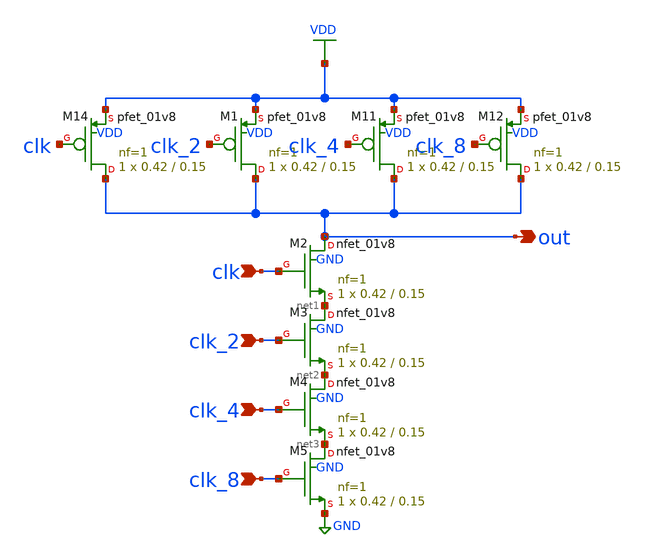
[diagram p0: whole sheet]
** sch_path: xschem/and_set/and_4.sch
**.subckt and_4 clk_2 clk clk_4 clk_8 out
*.ipin clk_2
*.ipin clk
*.ipin clk_4
*.ipin clk_8
*.opin out
XM1 out clk_2 VDD VDD sky130_fd_pr__pfet_01v8 L=0.15 W=0.42 nf=1 ad='int((nf+1)/2) * W/nf * 0.29' as='int((nf+2)/2) * W/nf * 0.29'
+ pd='2*int((nf+1)/2) * (W/nf + 0.29)' ps='2*int((nf+2)/2) * (W/nf + 0.29)' nrd='0.29 / W' nrs='0.29 / W'
+ sa=0 sb=0 sd=0 mult=1 m=1
XM2 out clk net1 GND sky130_fd_pr__nfet_01v8 L=0.15 W=0.42 nf=1 ad='int((nf+1)/2) * W/nf * 0.29' as='int((nf+2)/2) * W/nf * 0.29'
+ pd='2*int((nf+1)/2) * (W/nf + 0.29)' ps='2*int((nf+2)/2) * (W/nf + 0.29)' nrd='0.29 / W' nrs='0.29 / W'
+ sa=0 sb=0 sd=0 mult=1 m=1
XM3 net1 clk_2 net2 GND sky130_fd_pr__nfet_01v8 L=0.15 W=0.42 nf=1 ad='int((nf+1)/2) * W/nf * 0.29' as='int((nf+2)/2) * W/nf * 0.29'
+ pd='2*int((nf+1)/2) * (W/nf + 0.29)' ps='2*int((nf+2)/2) * (W/nf + 0.29)' nrd='0.29 / W' nrs='0.29 / W'
+ sa=0 sb=0 sd=0 mult=1 m=1
XM4 net2 clk_4 net3 GND sky130_fd_pr__nfet_01v8 L=0.15 W=0.42 nf=1 ad='int((nf+1)/2) * W/nf * 0.29' as='int((nf+2)/2) * W/nf * 0.29'
+ pd='2*int((nf+1)/2) * (W/nf + 0.29)' ps='2*int((nf+2)/2) * (W/nf + 0.29)' nrd='0.29 / W' nrs='0.29 / W'
+ sa=0 sb=0 sd=0 mult=1 m=1
XM5 net3 clk_8 GND GND sky130_fd_pr__nfet_01v8 L=0.15 W=0.42 nf=1 ad='int((nf+1)/2) * W/nf * 0.29' as='int((nf+2)/2) * W/nf * 0.29'
+ pd='2*int((nf+1)/2) * (W/nf + 0.29)' ps='2*int((nf+2)/2) * (W/nf + 0.29)' nrd='0.29 / W' nrs='0.29 / W'
+ sa=0 sb=0 sd=0 mult=1 m=1
XM11 out clk_4 VDD VDD sky130_fd_pr__pfet_01v8 L=0.15 W=0.42 nf=1 ad='int((nf+1)/2) * W/nf * 0.29' as='int((nf+2)/2) * W/nf * 0.29'
+ pd='2*int((nf+1)/2) * (W/nf + 0.29)' ps='2*int((nf+2)/2) * (W/nf + 0.29)' nrd='0.29 / W' nrs='0.29 / W'
+ sa=0 sb=0 sd=0 mult=1 m=1
XM12 out clk_8 VDD VDD sky130_fd_pr__pfet_01v8 L=0.15 W=0.42 nf=1 ad='int((nf+1)/2) * W/nf * 0.29' as='int((nf+2)/2) * W/nf * 0.29'
+ pd='2*int((nf+1)/2) * (W/nf + 0.29)' ps='2*int((nf+2)/2) * (W/nf + 0.29)' nrd='0.29 / W' nrs='0.29 / W'
+ sa=0 sb=0 sd=0 mult=1 m=1
XM14 out clk VDD VDD sky130_fd_pr__pfet_01v8 L=0.15 W=0.42 nf=1 ad='int((nf+1)/2) * W/nf * 0.29' as='int((nf+2)/2) * W/nf * 0.29'
+ pd='2*int((nf+1)/2) * (W/nf + 0.29)' ps='2*int((nf+2)/2) * (W/nf + 0.29)' nrd='0.29 / W' nrs='0.29 / W'
+ sa=0 sb=0 sd=0 mult=1 m=1
**.ends
.GLOBAL VDD
.GLOBAL GND
.end
